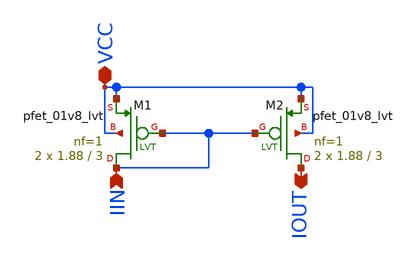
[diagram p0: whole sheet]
** sch_path: xschem/cmirror.sch
**.subckt cmirror IIN VCC IOUT
*.ipin IIN
*.iopin VCC
*.opin IOUT
XM1 IIN IIN VCC VCC sky130_fd_pr__pfet_01v8_lvt L=3 W=1.88 nf=1 ad='int((nf+1)/2) * W/nf * 0.29' as='int((nf+2)/2) * W/nf * 0.29'
+ pd='2*int((nf+1)/2) * (W/nf + 0.29)' ps='2*int((nf+2)/2) * (W/nf + 0.29)' nrd='0.29 / W' nrs='0.29 / W'
+ sa=0 sb=0 sd=0 mult=2 m=2
XM2 IOUT IIN VCC VCC sky130_fd_pr__pfet_01v8_lvt L=3 W=1.88 nf=1 ad='int((nf+1)/2) * W/nf * 0.29' as='int((nf+2)/2) * W/nf * 0.29'
+ pd='2*int((nf+1)/2) * (W/nf + 0.29)' ps='2*int((nf+2)/2) * (W/nf + 0.29)' nrd='0.29 / W' nrs='0.29 / W'
+ sa=0 sb=0 sd=0 mult=2 m=2
**.ends
.end
